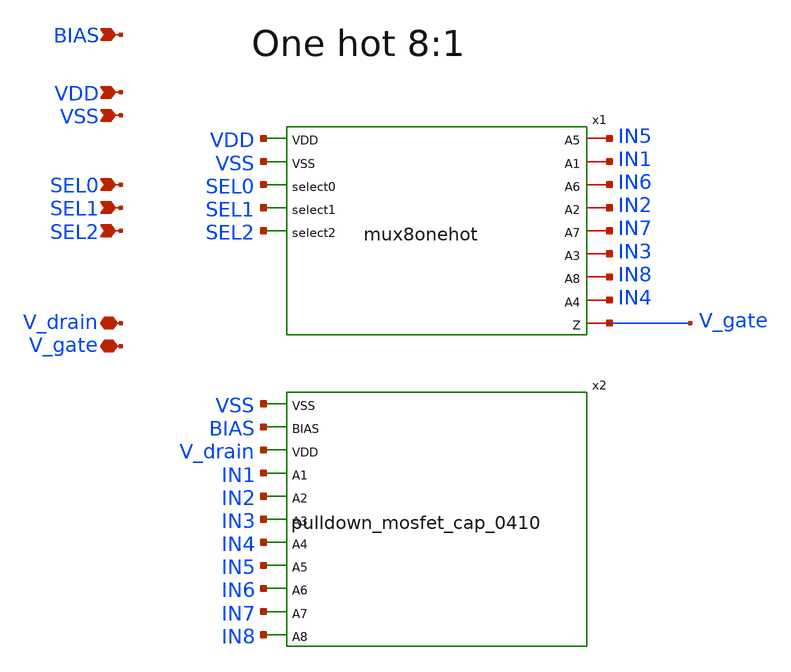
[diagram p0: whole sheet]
** sch_path: sch/mux8onehot_cap_0410.sch
**.subckt mux8onehot_cap_0410 SEL0 SEL1 SEL2 VDD VSS V_gate BIAS V_drain
*.ipin SEL0
*.ipin SEL1
*.ipin SEL2
*.ipin VDD
*.ipin VSS
*.iopin V_gate
*.ipin BIAS
*.iopin V_drain
x1 VDD VSS SEL0 SEL1 IN5 SEL2 IN1 IN6 IN2 IN7 IN3 IN8 IN4 V_gate mux8onehot
x2 VSS BIAS V_drain IN1 IN2 IN3 IN4 IN5 IN6 IN7 IN8 pulldown_mosfet_cap_0410
**.ends
.end
